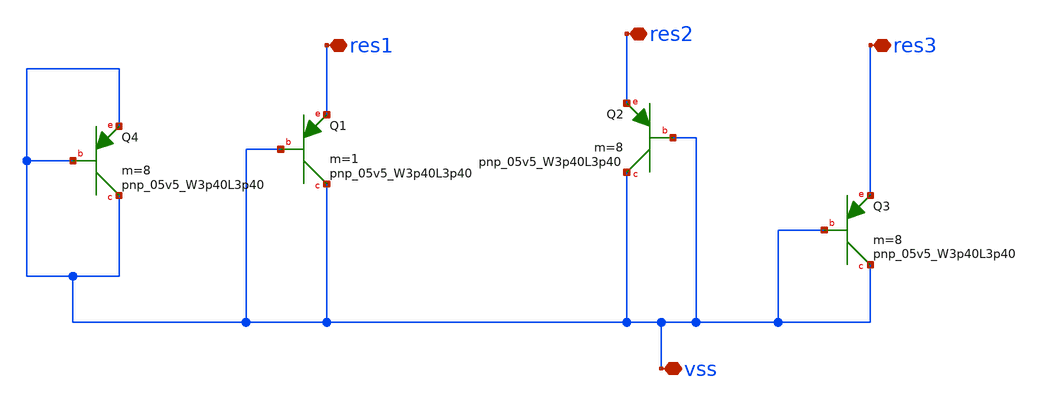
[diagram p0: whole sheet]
** sch_path: BGR_NSL/test/bjt_cont.sch
**.subckt bjt_cont vss res1 res2 res3
*.iopin vss
*.iopin res1
*.iopin res2
*.iopin res3
XQ1 vss vss res1 sky130_fd_pr__pnp_05v5_W3p40L3p40 m=1
XQ2 vss vss res2 sky130_fd_pr__pnp_05v5_W3p40L3p40 m=8
XQ3 vss vss res3 sky130_fd_pr__pnp_05v5_W3p40L3p40 m=8
XQ4 vss vss vss sky130_fd_pr__pnp_05v5_W3p40L3p40 m=8
**.ends
.end
